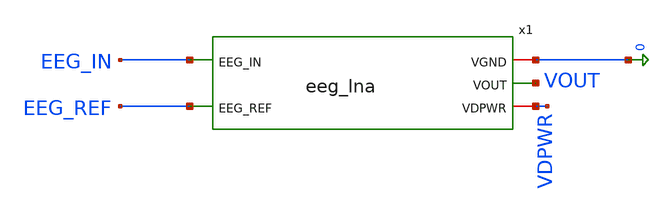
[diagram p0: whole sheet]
** sch_path: xschem/eeg_lna_tb.sch
**.subckt eeg_lna_tb
x1 EEG_IN EEG_REF 0 VOUT VDPWR eeg_lna
**** begin user architecture code


.lib /foss/pdks/sky130A/libs.tech/ngspice/sky130.lib.spice tt

.option rshunt=1e15
.option savecurrents

* =====================================================
* INPUT SIGNALS
* =====================================================

V1 EEG_IN EEG_REF SIN(0 1m 10) DC 0 AC 1
V2 VDPWR 0 DC 1.8

RREF EEG_REF 0 100k

* =====================================================
* ANALYSIS CONTROL
* =====================================================

.control

destroy all
save all

echo "======================================="
echo "EEG LNA DEBUG REPORT"
echo "======================================="

* =====================================================
* OPERATING POINT
* =====================================================

op

echo "======================================="
echo "OPERATING POINT"
echo "======================================="

print v(vout)
print v(eeg_in)
print v(eeg_ref)

* IMPORTANT INTERNAL NODES
* Change names if needed to match your schematic
print v(x1.vin_p)
print v(x1.vin_n)

print v(x1.tail_p)
print v(x1.mirror_bias_n)
print v(x1.bias_p)

print i(v2)

* =====================================================
* DEVICE OPERATING INFO
* =====================================================

echo "======================================="
echo "MOSFET OPERATING REGIONS"
echo "======================================="

show m.x1.xm1.msky130_fd_pr__nfet_01v8
show m.x1.xm2.msky130_fd_pr__nfet_01v8
show m.x1.xm3.msky130_fd_pr__pfet_01v8
show m.x1.xm4.msky130_fd_pr__pfet_01v8
show m.x1.xm5.msky130_fd_pr__pfet_01v8
show m.x1.xm6.msky130_fd_pr__pfet_01v8
show m.x1.xm7.msky130_fd_pr__nfet_01v8

* =====================================================
* TRANSIENT
* =====================================================

echo "======================================="
echo "TRANSIENT ANALYSIS"
echo "======================================="

tran 100u 200m

plot v(eeg_in)-v(eeg_ref)
plot v(eeg_ref)
plot v(vout)

* DIFFERENTIAL INPUT CHECK
plot v(x1.vin_p)-v(x1.vin_n)

* OUTPUT SWING AROUND BIAS
plot v(vout)-avg(v(vout))

* =====================================================
* AC ANALYSIS
* =====================================================

echo "======================================="
echo "AC ANALYSIS"
echo "======================================="

ac dec 20 0.1 10k

* External transfer
plot db(v(vout)/(v(eeg_in)-v(eeg_ref)))

* Internal OTA gain
plot db(v(vout)/v(x1.vin_p))

* Differential gain
plot db(v(vout)/(v(x1.vin_p)-v(x1.vin_n)))

* =====================================================
* NOISE ANALYSIS
* =====================================================

echo "======================================="
echo "NOISE ANALYSIS"
echo "======================================="

noise v(vout) V1 dec 20 0.1 10k 1

setplot noise1

display

* TOTAL OUTPUT NOISE
plot onoise_spectrum xlog ylog

* INPUT REFERRED NOISE
plot inoise_spectrum xlog ylog

* ALL CONTRIBUTORS
plot all xlog ylog

print all

* =====================================================
* SAVE RAW
* =====================================================

write lna_tb.raw

.endc

.end


**** end user architecture code
**.ends

* expanding   symbol:  eeg_lna.sym # of pins=5
** sym_path: xschem/eeg_lna.sym
** sch_path: xschem/eeg_lna.sch
.subckt eeg_lna EEG_IN EEG_REF VGND VOUT VDPWR
*.iopin VGND
*.ipin EEG_REF
*.ipin EEG_IN
*.iopin VDPWR
*.opin VOUT
XM1 MIRROR_BIAS_N MIRROR_BIAS_N VGND VGND sky130_fd_pr__nfet_01v8 L=1.0 W=40 nf=1 ad='int((1 + 1)/2) * 40 / 1 * 0.29'
+ as='int((1 + 2)/2) * 40 / 1 * 0.29' pd='2*int((1 + 1)/2) * (40 / 1 + 0.29)' ps='2*int((1 + 2)/2) * (40 / 1 + 0.29)'
+ nrd='0.29 / 40 ' nrs='0.29 / 40 ' sa=0 sb=0 sd=0 mult=1 m=1
XM2 VOUT MIRROR_BIAS_N VGND VGND sky130_fd_pr__nfet_01v8 L=1.0 W=40 nf=1 ad='int((1 + 1)/2) * 40 / 1 * 0.29'
+ as='int((1 + 2)/2) * 40 / 1 * 0.29' pd='2*int((1 + 1)/2) * (40 / 1 + 0.29)' ps='2*int((1 + 2)/2) * (40 / 1 + 0.29)'
+ nrd='0.29 / 40 ' nrs='0.29 / 40 ' sa=0 sb=0 sd=0 mult=1 m=1
XM3 MIRROR_BIAS_N VIN_P TAIL_P VDPWR sky130_fd_pr__pfet_01v8 L=1.0 W=60 nf=1 ad='int((1 + 1)/2) * 60 / 1 * 0.29'
+ as='int((1 + 2)/2) * 60 / 1 * 0.29' pd='2*int((1 + 1)/2) * (60 / 1 + 0.29)' ps='2*int((1 + 2)/2) * (60 / 1 + 0.29)'
+ nrd='0.29 / 60 ' nrs='0.29 / 60 ' sa=0 sb=0 sd=0 mult=1 m=1
XM4 VOUT VIN_N TAIL_P VDPWR sky130_fd_pr__pfet_01v8 L=1.0 W=60 nf=1 ad='int((1 + 1)/2) * 60 / 1 * 0.29'
+ as='int((1 + 2)/2) * 60 / 1 * 0.29' pd='2*int((1 + 1)/2) * (60 / 1 + 0.29)' ps='2*int((1 + 2)/2) * (60 / 1 + 0.29)'
+ nrd='0.29 / 60 ' nrs='0.29 / 60 ' sa=0 sb=0 sd=0 mult=1 m=1
XM5 TAIL_P BIAS_P VDPWR VDPWR sky130_fd_pr__pfet_01v8 L=1.0 W=15 nf=1 ad='int((1 + 1)/2) * 15 / 1 * 0.29'
+ as='int((1 + 2)/2) * 15 / 1 * 0.29' pd='2*int((1 + 1)/2) * (15 / 1 + 0.29)' ps='2*int((1 + 2)/2) * (15 / 1 + 0.29)'
+ nrd='0.29 / 15 ' nrs='0.29 / 15 ' sa=0 sb=0 sd=0 mult=1 m=1
XM6 BIAS_P BIAS_P VDPWR VDPWR sky130_fd_pr__pfet_01v8 L=1.0 W=10 nf=1 ad='int((1 + 1)/2) * 10 / 1 * 0.29'
+ as='int((1 + 2)/2) * 10 / 1 * 0.29' pd='2*int((1 + 1)/2) * (10 / 1 + 0.29)' ps='2*int((1 + 2)/2) * (10 / 1 + 0.29)'
+ nrd='0.29 / 10 ' nrs='0.29 / 10 ' sa=0 sb=0 sd=0 mult=1 m=1
XM7 BIAS_P BIAS_P VGND VGND sky130_fd_pr__nfet_01v8 L=1.0 W=5 nf=1 ad='int((1 + 1)/2) * 5 / 1 * 0.29'
+ as='int((1 + 2)/2) * 5 / 1 * 0.29' pd='2*int((1 + 1)/2) * (5 / 1 + 0.29)' ps='2*int((1 + 2)/2) * (5 / 1 + 0.29)'
+ nrd='0.29 / 5 ' nrs='0.29 / 5 ' sa=0 sb=0 sd=0 mult=1 m=1
XCIN EEG_IN VIN_N sky130_fd_pr__cap_mim_m3_1 W=40 L=40 MF=1 m=1
XCREF EEG_REF VIN_P sky130_fd_pr__cap_mim_m3_1 W=40 L=40 MF=1 m=1
xpinbias VIN_P BIAS_P pseudo_res
x2 VOUT VIN_N pseudo_res
XC1 VOUT VIN_N sky130_fd_pr__cap_mim_m3_1 W=5 L=5 MF=1 m=1
.ends


* expanding   symbol:  pseudo_res.sym # of pins=2
** sym_path: xschem/pseudo_res.sym
** sch_path: xschem/pseudo_res.sch
.subckt pseudo_res B A
*.iopin A
*.iopin B
XM1_PSEUDO_RES B B A A sky130_fd_pr__pfet_01v8 L=10 W=0.42 nf=1 ad='int((1 + 1)/2) * 0.42 / 1 * 0.29'
+ as='int((1 + 2)/2) * 0.42 / 1 * 0.29' pd='2*int((1 + 1)/2) * (0.42 / 1 + 0.29)' ps='2*int((1 + 2)/2) * (0.42 / 1 + 0.29)'
+ nrd='0.29 / 0.42 ' nrs='0.29 / 0.42 ' sa=0 sb=0 sd=0 mult=1 m=1
XM2_PSEUDO_RES A A B B sky130_fd_pr__pfet_01v8 L=10 W=0.42 nf=1 ad='int((1 + 1)/2) * 0.42 / 1 * 0.29'
+ as='int((1 + 2)/2) * 0.42 / 1 * 0.29' pd='2*int((1 + 1)/2) * (0.42 / 1 + 0.29)' ps='2*int((1 + 2)/2) * (0.42 / 1 + 0.29)'
+ nrd='0.29 / 0.42 ' nrs='0.29 / 0.42 ' sa=0 sb=0 sd=0 mult=1 m=1
.ends

.end
